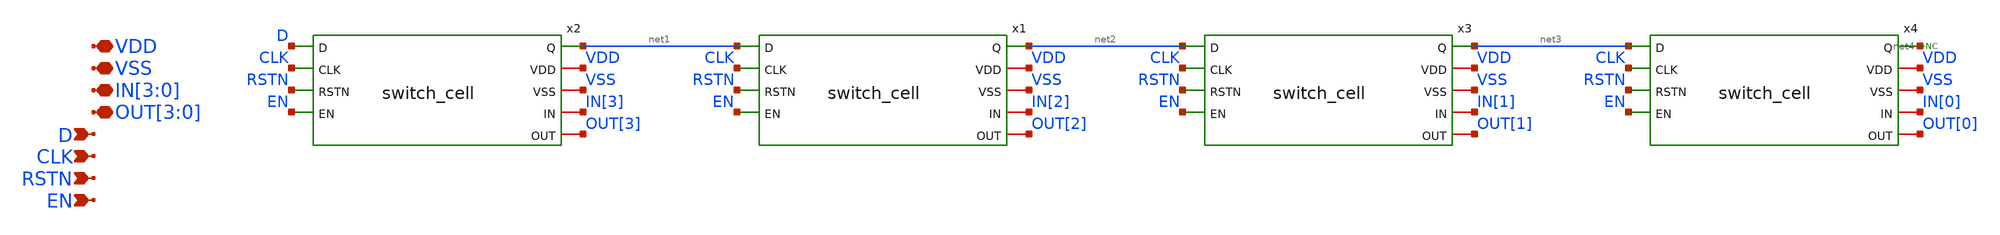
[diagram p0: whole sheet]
** sch_path: designs/libs/core_analog/switch-matrix/tg_array_4x1.sch
**.subckt tg_array_4x1 VDD VSS IN[3],IN[2],IN[1],IN[0] OUT[3],OUT[2],OUT[1],OUT[0] D RSTN CLK EN
*.iopin VDD
*.iopin VSS
*.iopin IN[3],IN[2],IN[1],IN[0]
*.iopin OUT[3],OUT[2],OUT[1],OUT[0]
*.ipin D
*.ipin RSTN
*.ipin CLK
*.ipin EN
x2 net1 VDD VSS D CLK RSTN EN IN[3] OUT[3] switch_cell
x1 net2 VDD VSS net1 CLK RSTN EN IN[2] OUT[2] switch_cell
x3 net3 VDD VSS net2 CLK RSTN EN IN[1] OUT[1] switch_cell
x4 net4 VDD VSS net3 CLK RSTN EN IN[0] OUT[0] switch_cell
* noconn #net4
**.ends
.end
